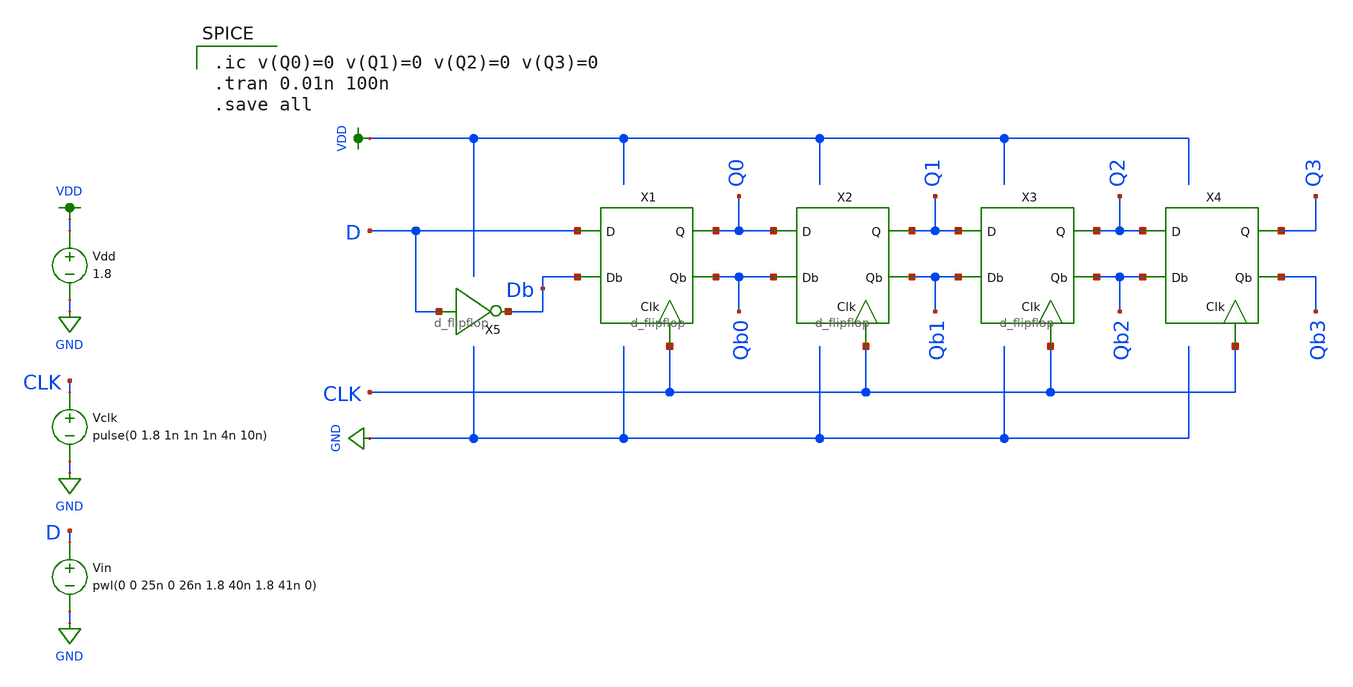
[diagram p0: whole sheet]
** sch_path: simulation/shift_register/simulations_andrew_files/shift_register_tran_4bit_andrew.sch
**.subckt shift_register_tran_4bit_andrew
X1 D Db CLK Qb0 Q0 d_flipflop
X2 Q0 Qb0 CLK Qb1 Q1 d_flipflop
X3 Q1 Qb1 CLK Qb2 Q2 d_flipflop
X4 Q2 Qb2 CLK Qb3 Q3 d_flipflop
X5 D Db sreg_inverter
Vdd VDD GND 1.8
Vclk CLK GND pulse(0 1.8 1n 1n 1n 4n 10n)
Vin D GND pwl(0 0 25n 0 26n 1.8 40n 1.8 41n 0)
**** begin user architecture code

.ic v(Q0)=0 v(Q1)=0 v(Q2)=0 v(Q3)=0
.tran 0.01n 100n
.save all


.option wnflag=1
.param MC_SWITCH=0.0
.lib ~/skywater/skywater-pdk/libraries/sky130_fd_pr_ngspice/latest/models/sky130.lib.spice tt

**** end user architecture code
**.ends

* expanding   symbol:
*+  /home/madvlsi/Documents/VLSI_Sine_Gen/simulation/shift_register/andrew_mp2_files/d_flipflop/d_flipflop.sym # of pins=5
** sym_path: simulation/shift_register/andrew_mp2_files/d_flipflop/d_flipflop.sym
** sch_path: simulation/shift_register/andrew_mp2_files/d_flipflop/d_flipflop.sch
.subckt d_flipflop D Db CLK Qb Q
*.ipin D
*.ipin CLK
*.opin Q
*.opin Qb
*.ipin Db
XM1 D CLK net2 VP sky130_fd_pr__pfet_01v8 L=0.15 W=1 nf=1 ad='int((nf+1)/2) * W/nf * 0.29' as='int((nf+2)/2) * W/nf * 0.29'
+ pd='2*int((nf+1)/2) * (W/nf + 0.29)' ps='2*int((nf+2)/2) * (W/nf + 0.29)' nrd='0.29 / W' nrs='0.29 / W'
+ sa=0 sb=0 sd=0 mult=1 m=1
XM2 Db CLK net3 VP sky130_fd_pr__pfet_01v8 L=0.15 W=1 nf=1 ad='int((nf+1)/2) * W/nf * 0.29' as='int((nf+2)/2) * W/nf * 0.29'
+ pd='2*int((nf+1)/2) * (W/nf + 0.29)' ps='2*int((nf+2)/2) * (W/nf + 0.29)' nrd='0.29 / W' nrs='0.29 / W'
+ sa=0 sb=0 sd=0 mult=1 m=1
XM3 VDD net2 net3 VP sky130_fd_pr__pfet_01v8 L=0.15 W=1 nf=1 ad='int((nf+1)/2) * W/nf * 0.29' as='int((nf+2)/2) * W/nf * 0.29'
+ pd='2*int((nf+1)/2) * (W/nf + 0.29)' ps='2*int((nf+2)/2) * (W/nf + 0.29)' nrd='0.29 / W' nrs='0.29 / W'
+ sa=0 sb=0 sd=0 mult=1 m=1
XM5 net3 net2 net1 VN sky130_fd_pr__nfet_01v8 L=0.15 W=1 nf=1 ad='int((nf+1)/2) * W/nf * 0.29' as='int((nf+2)/2) * W/nf * 0.29'
+ pd='2*int((nf+1)/2) * (W/nf + 0.29)' ps='2*int((nf+2)/2) * (W/nf + 0.29)' nrd='0.29 / W' nrs='0.29 / W'
+ sa=0 sb=0 sd=0 mult=1 m=1
XM7 net1 CLK GND VN sky130_fd_pr__nfet_01v8 L=0.15 W=4 nf=1 ad='int((nf+1)/2) * W/nf * 0.29' as='int((nf+2)/2) * W/nf * 0.29'
+ pd='2*int((nf+1)/2) * (W/nf + 0.29)' ps='2*int((nf+2)/2) * (W/nf + 0.29)' nrd='0.29 / W' nrs='0.29 / W'
+ sa=0 sb=0 sd=0 mult=1 m=1
XM8 Q CLK net2 VN sky130_fd_pr__nfet_01v8 L=0.15 W=1 nf=1 ad='int((nf+1)/2) * W/nf * 0.29' as='int((nf+2)/2) * W/nf * 0.29'
+ pd='2*int((nf+1)/2) * (W/nf + 0.29)' ps='2*int((nf+2)/2) * (W/nf + 0.29)' nrd='0.29 / W' nrs='0.29 / W'
+ sa=0 sb=0 sd=0 mult=1 m=1
XM9 Qb CLK net3 VN sky130_fd_pr__nfet_01v8 L=0.15 W=1 nf=1 ad='int((nf+1)/2) * W/nf * 0.29' as='int((nf+2)/2) * W/nf * 0.29'
+ pd='2*int((nf+1)/2) * (W/nf + 0.29)' ps='2*int((nf+2)/2) * (W/nf + 0.29)' nrd='0.29 / W' nrs='0.29 / W'
+ sa=0 sb=0 sd=0 mult=1 m=1
XM10 net4 Q Qb VP sky130_fd_pr__pfet_01v8 L=0.15 W=1 nf=1 ad='int((nf+1)/2) * W/nf * 0.29' as='int((nf+2)/2) * W/nf * 0.29'
+ pd='2*int((nf+1)/2) * (W/nf + 0.29)' ps='2*int((nf+2)/2) * (W/nf + 0.29)' nrd='0.29 / W' nrs='0.29 / W'
+ sa=0 sb=0 sd=0 mult=1 m=1
XM11 net4 Qb Q VP sky130_fd_pr__pfet_01v8 L=0.15 W=1 nf=1 ad='int((nf+1)/2) * W/nf * 0.29' as='int((nf+2)/2) * W/nf * 0.29'
+ pd='2*int((nf+1)/2) * (W/nf + 0.29)' ps='2*int((nf+2)/2) * (W/nf + 0.29)' nrd='0.29 / W' nrs='0.29 / W'
+ sa=0 sb=0 sd=0 mult=1 m=1
XM12 VDD CLK net4 VP sky130_fd_pr__pfet_01v8 L=0.15 W=4 nf=1 ad='int((nf+1)/2) * W/nf * 0.29' as='int((nf+2)/2) * W/nf * 0.29'
+ pd='2*int((nf+1)/2) * (W/nf + 0.29)' ps='2*int((nf+2)/2) * (W/nf + 0.29)' nrd='0.29 / W' nrs='0.29 / W'
+ sa=0 sb=0 sd=0 mult=1 m=1
XM13 Qb Q GND VN sky130_fd_pr__nfet_01v8 L=0.15 W=1 nf=1 ad='int((nf+1)/2) * W/nf * 0.29' as='int((nf+2)/2) * W/nf * 0.29'
+ pd='2*int((nf+1)/2) * (W/nf + 0.29)' ps='2*int((nf+2)/2) * (W/nf + 0.29)' nrd='0.29 / W' nrs='0.29 / W'
+ sa=0 sb=0 sd=0 mult=1 m=1
XM14 Q Qb GND VN sky130_fd_pr__nfet_01v8 L=0.15 W=1 nf=1 ad='int((nf+1)/2) * W/nf * 0.29' as='int((nf+2)/2) * W/nf * 0.29'
+ pd='2*int((nf+1)/2) * (W/nf + 0.29)' ps='2*int((nf+2)/2) * (W/nf + 0.29)' nrd='0.29 / W' nrs='0.29 / W'
+ sa=0 sb=0 sd=0 mult=1 m=1
XM4 VDD net3 net2 VP sky130_fd_pr__pfet_01v8 L=0.15 W=1 nf=1 ad='int((nf+1)/2) * W/nf * 0.29' as='int((nf+2)/2) * W/nf * 0.29'
+ pd='2*int((nf+1)/2) * (W/nf + 0.29)' ps='2*int((nf+2)/2) * (W/nf + 0.29)' nrd='0.29 / W' nrs='0.29 / W'
+ sa=0 sb=0 sd=0 mult=1 m=1
XM6 net2 net3 net1 VN sky130_fd_pr__nfet_01v8 L=0.15 W=1 nf=1 ad='int((nf+1)/2) * W/nf * 0.29' as='int((nf+2)/2) * W/nf * 0.29'
+ pd='2*int((nf+1)/2) * (W/nf + 0.29)' ps='2*int((nf+2)/2) * (W/nf + 0.29)' nrd='0.29 / W' nrs='0.29 / W'
+ sa=0 sb=0 sd=0 mult=1 m=1
.ends


* expanding   symbol:
*+  /home/madvlsi/Documents/VLSI_Sine_Gen/simulation/shift_register/andrew_mp2_files/sreg_inverter/sreg_inverter.sym # of pins=2
** sym_path: simulation/shift_register/andrew_mp2_files/sreg_inverter/sreg_inverter.sym
** sch_path: simulation/shift_register/andrew_mp2_files/sreg_inverter/sreg_inverter.sch
.subckt sreg_inverter A Y
*.ipin A
*.opin Y
XM1 Y A GND GND sky130_fd_pr__nfet_01v8 L=0.15 W=1 nf=1 ad='int((nf+1)/2) * W/nf * 0.29' as='int((nf+2)/2) * W/nf * 0.29'
+ pd='2*int((nf+1)/2) * (W/nf + 0.29)' ps='2*int((nf+2)/2) * (W/nf + 0.29)' nrd='0.29 / W' nrs='0.29 / W'
+ sa=0 sb=0 sd=0 mult=1 m=1
XM2 Y A VDD VDD sky130_fd_pr__pfet_01v8 L=0.15 W=1 nf=1 ad='int((nf+1)/2) * W/nf * 0.29' as='int((nf+2)/2) * W/nf * 0.29'
+ pd='2*int((nf+1)/2) * (W/nf + 0.29)' ps='2*int((nf+2)/2) * (W/nf + 0.29)' nrd='0.29 / W' nrs='0.29 / W'
+ sa=0 sb=0 sd=0 mult=1 m=1
.ends

.GLOBAL VDD
.GLOBAL GND
.end
